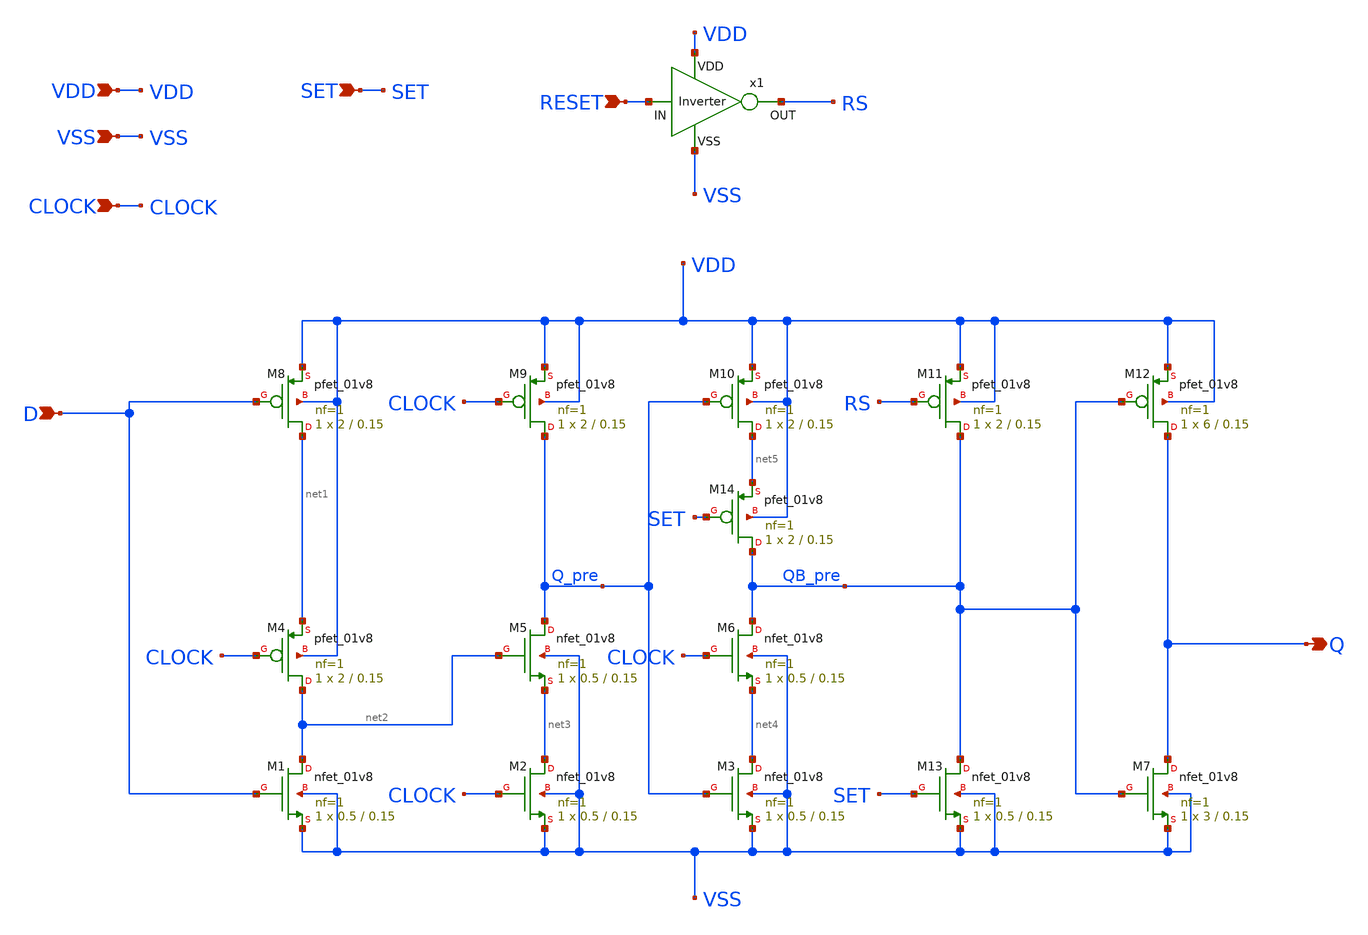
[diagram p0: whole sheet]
** sch_path: FFD_TSPC.sch
**.subckt FFD_TSPC CLOCK SET RESET VDD VSS D Q
*.ipin CLOCK
*.ipin SET
*.ipin RESET
*.ipin VDD
*.ipin VSS
*.ipin D
*.opin Q
XM1 net2 D VSS VSS sky130_fd_pr__nfet_01v8 L=0.15 W=0.5 nf=1 ad='int((nf+1)/2) * W/nf * 0.29' as='int((nf+2)/2) * W/nf * 0.29'
+ pd='2*int((nf+1)/2) * (W/nf + 0.29)' ps='2*int((nf+2)/2) * (W/nf + 0.29)' nrd='0.29 / W' nrs='0.29 / W'
+ sa=0 sb=0 sd=0 mult=1 m=1
XM2 net3 CLOCK VSS VSS sky130_fd_pr__nfet_01v8 L=0.15 W=0.5 nf=1 ad='int((nf+1)/2) * W/nf * 0.29' as='int((nf+2)/2) * W/nf * 0.29'
+ pd='2*int((nf+1)/2) * (W/nf + 0.29)' ps='2*int((nf+2)/2) * (W/nf + 0.29)' nrd='0.29 / W' nrs='0.29 / W'
+ sa=0 sb=0 sd=0 mult=1 m=1
XM3 net4 Q_pre VSS VSS sky130_fd_pr__nfet_01v8 L=0.15 W=0.5 nf=1 ad='int((nf+1)/2) * W/nf * 0.29' as='int((nf+2)/2) * W/nf * 0.29'
+ pd='2*int((nf+1)/2) * (W/nf + 0.29)' ps='2*int((nf+2)/2) * (W/nf + 0.29)' nrd='0.29 / W' nrs='0.29 / W'
+ sa=0 sb=0 sd=0 mult=1 m=1
XM4 net2 CLOCK net1 VDD sky130_fd_pr__pfet_01v8 L=0.15 W=2 nf=1 ad='int((nf+1)/2) * W/nf * 0.29' as='int((nf+2)/2) * W/nf * 0.29'
+ pd='2*int((nf+1)/2) * (W/nf + 0.29)' ps='2*int((nf+2)/2) * (W/nf + 0.29)' nrd='0.29 / W' nrs='0.29 / W'
+ sa=0 sb=0 sd=0 mult=1 m=1
XM5 Q_pre net2 net3 VSS sky130_fd_pr__nfet_01v8 L=0.15 W=0.5 nf=1 ad='int((nf+1)/2) * W/nf * 0.29' as='int((nf+2)/2) * W/nf * 0.29'
+ pd='2*int((nf+1)/2) * (W/nf + 0.29)' ps='2*int((nf+2)/2) * (W/nf + 0.29)' nrd='0.29 / W' nrs='0.29 / W'
+ sa=0 sb=0 sd=0 mult=1 m=1
XM6 QB_pre CLOCK net4 VSS sky130_fd_pr__nfet_01v8 L=0.15 W=0.5 nf=1 ad='int((nf+1)/2) * W/nf * 0.29'
+ as='int((nf+2)/2) * W/nf * 0.29' pd='2*int((nf+1)/2) * (W/nf + 0.29)' ps='2*int((nf+2)/2) * (W/nf + 0.29)'
+ nrd='0.29 / W' nrs='0.29 / W' sa=0 sb=0 sd=0 mult=1 m=1
XM7 Q QB_pre VSS VSS sky130_fd_pr__nfet_01v8 L=0.15 W=3 nf=1 ad='int((nf+1)/2) * W/nf * 0.29' as='int((nf+2)/2) * W/nf * 0.29'
+ pd='2*int((nf+1)/2) * (W/nf + 0.29)' ps='2*int((nf+2)/2) * (W/nf + 0.29)' nrd='0.29 / W' nrs='0.29 / W'
+ sa=0 sb=0 sd=0 mult=1 m=1
XM8 net1 D VDD VDD sky130_fd_pr__pfet_01v8 L=0.15 W=2 nf=1 ad='int((nf+1)/2) * W/nf * 0.29' as='int((nf+2)/2) * W/nf * 0.29'
+ pd='2*int((nf+1)/2) * (W/nf + 0.29)' ps='2*int((nf+2)/2) * (W/nf + 0.29)' nrd='0.29 / W' nrs='0.29 / W'
+ sa=0 sb=0 sd=0 mult=1 m=1
XM9 Q_pre CLOCK VDD VDD sky130_fd_pr__pfet_01v8 L=0.15 W=2 nf=1 ad='int((nf+1)/2) * W/nf * 0.29' as='int((nf+2)/2) * W/nf * 0.29'
+ pd='2*int((nf+1)/2) * (W/nf + 0.29)' ps='2*int((nf+2)/2) * (W/nf + 0.29)' nrd='0.29 / W' nrs='0.29 / W'
+ sa=0 sb=0 sd=0 mult=1 m=1
XM10 net5 Q_pre VDD VDD sky130_fd_pr__pfet_01v8 L=0.15 W=2 nf=1 ad='int((nf+1)/2) * W/nf * 0.29' as='int((nf+2)/2) * W/nf * 0.29'
+ pd='2*int((nf+1)/2) * (W/nf + 0.29)' ps='2*int((nf+2)/2) * (W/nf + 0.29)' nrd='0.29 / W' nrs='0.29 / W'
+ sa=0 sb=0 sd=0 mult=1 m=1
XM11 QB_pre RS VDD VDD sky130_fd_pr__pfet_01v8 L=0.15 W=2 nf=1 ad='int((nf+1)/2) * W/nf * 0.29' as='int((nf+2)/2) * W/nf * 0.29'
+ pd='2*int((nf+1)/2) * (W/nf + 0.29)' ps='2*int((nf+2)/2) * (W/nf + 0.29)' nrd='0.29 / W' nrs='0.29 / W'
+ sa=0 sb=0 sd=0 mult=1 m=1
XM12 Q QB_pre VDD VDD sky130_fd_pr__pfet_01v8 L=0.15 W=6 nf=1 ad='int((nf+1)/2) * W/nf * 0.29' as='int((nf+2)/2) * W/nf * 0.29'
+ pd='2*int((nf+1)/2) * (W/nf + 0.29)' ps='2*int((nf+2)/2) * (W/nf + 0.29)' nrd='0.29 / W' nrs='0.29 / W'
+ sa=0 sb=0 sd=0 mult=1 m=1
XM13 QB_pre SET VSS VSS sky130_fd_pr__nfet_01v8 L=0.15 W=0.5 nf=1 ad='int((nf+1)/2) * W/nf * 0.29' as='int((nf+2)/2) * W/nf * 0.29'
+ pd='2*int((nf+1)/2) * (W/nf + 0.29)' ps='2*int((nf+2)/2) * (W/nf + 0.29)' nrd='0.29 / W' nrs='0.29 / W'
+ sa=0 sb=0 sd=0 mult=1 m=1
x1 VDD RESET RS VSS Inverter
XM14 QB_pre SET net5 VDD sky130_fd_pr__pfet_01v8 L=0.15 W=2 nf=1 ad='int((nf+1)/2) * W/nf * 0.29' as='int((nf+2)/2) * W/nf * 0.29'
+ pd='2*int((nf+1)/2) * (W/nf + 0.29)' ps='2*int((nf+2)/2) * (W/nf + 0.29)' nrd='0.29 / W' nrs='0.29 / W'
+ sa=0 sb=0 sd=0 mult=1 m=1
**.ends

* expanding   symbol:  Inverter.sym # of pins=4
** sym_path: Inverter.sym
** sch_path: Inverter.sch
.subckt Inverter VDD IN OUT VSS
*.ipin IN
*.ipin VSS
*.ipin VDD
*.opin OUT
XM1 OUT IN VSS VSS sky130_fd_pr__nfet_01v8 L=0.3 W=1 nf=1 ad='int((nf+1)/2) * W/nf * 0.29' as='int((nf+2)/2) * W/nf * 0.29'
+ pd='2*int((nf+1)/2) * (W/nf + 0.29)' ps='2*int((nf+2)/2) * (W/nf + 0.29)' nrd='0.29 / W' nrs='0.29 / W'
+ sa=0 sb=0 sd=0 mult=1 m=1
XM2 OUT IN VDD VDD sky130_fd_pr__pfet_01v8 L=0.3 W=2 nf=1 ad='int((nf+1)/2) * W/nf * 0.29' as='int((nf+2)/2) * W/nf * 0.29'
+ pd='2*int((nf+1)/2) * (W/nf + 0.29)' ps='2*int((nf+2)/2) * (W/nf + 0.29)' nrd='0.29 / W' nrs='0.29 / W'
+ sa=0 sb=0 sd=0 mult=1 m=1
.ends

.end
